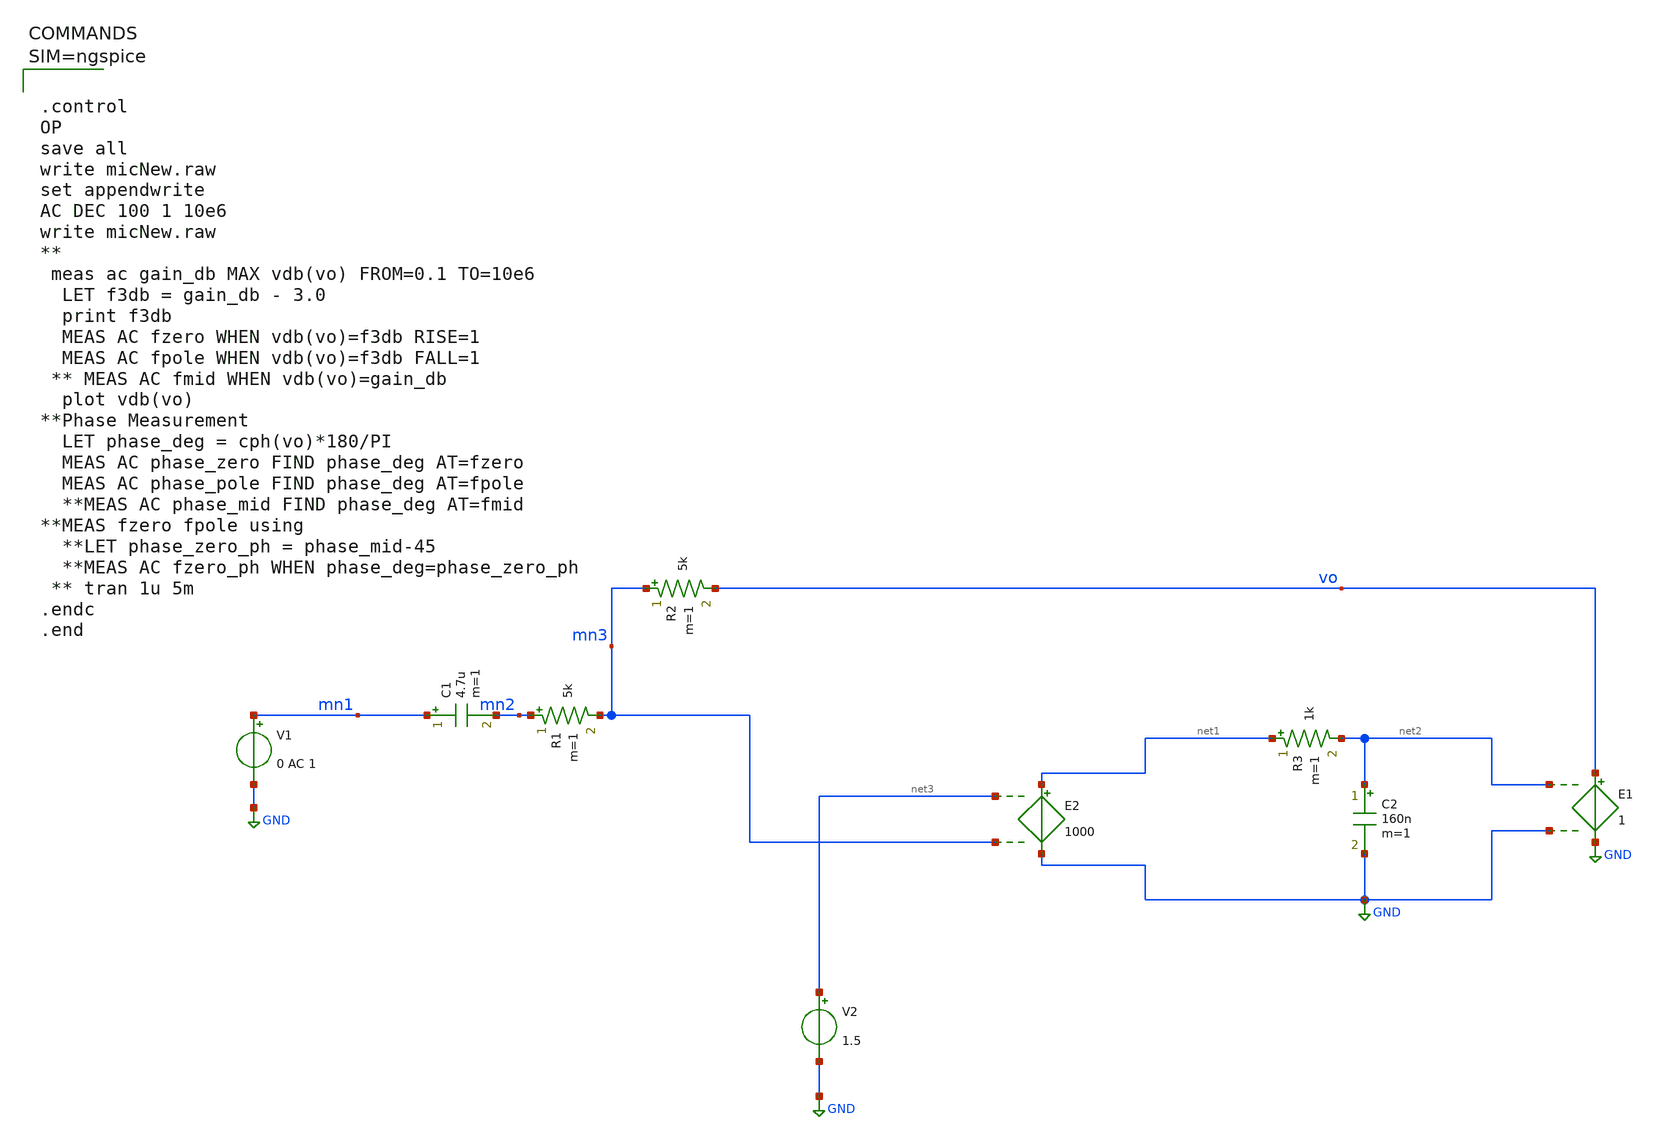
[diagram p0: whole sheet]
** sch_path: xschem/micNewOpa_mod2.sch
**.subckt micNewOpa_mod2
V1 mn1 GND 0 AC 1
C1 mn1 mn2 4.7u m=1
R1 mn2 mn3 5k m=1
R2 mn3 vo 5k m=1
V2 net3 GND 1.5
E2 net1 GND net3 mn3 1000
E1 vo GND net2 GND 1
R3 net1 net2 1k m=1
C2 net2 GND 160n m=1
**** begin user architecture code



.control
OP
save all
write micNew.raw
set appendwrite
AC DEC 100 1 10e6
write micNew.raw
**
 meas ac gain_db MAX vdb(vo) FROM=0.1 TO=10e6
  LET f3db = gain_db - 3.0
  print f3db
  MEAS AC fzero WHEN vdb(vo)=f3db RISE=1
  MEAS AC fpole WHEN vdb(vo)=f3db FALL=1
 ** MEAS AC fmid WHEN vdb(vo)=gain_db
  plot vdb(vo)
**Phase Measurement
  LET phase_deg = cph(vo)*180/PI
  MEAS AC phase_zero FIND phase_deg AT=fzero
  MEAS AC phase_pole FIND phase_deg AT=fpole
  **MEAS AC phase_mid FIND phase_deg AT=fmid
**MEAS fzero fpole using
  **LET phase_zero_ph = phase_mid-45
  **MEAS AC fzero_ph WHEN phase_deg=phase_zero_ph
 ** tran 1u 5m
.endc
.end



**** end user architecture code
**.ends
.GLOBAL GND
.end
